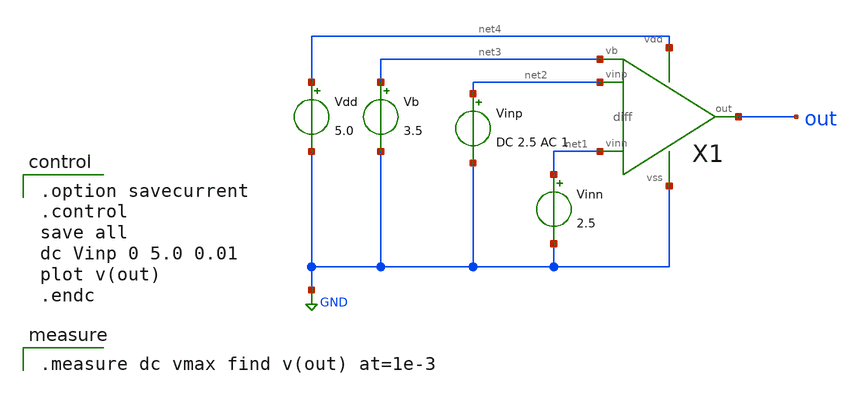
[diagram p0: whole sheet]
** sch_path: member_project/OPAMP/ShuntaroOhno/xschem/diff_dc.sch
**.subckt diff_dc
Vdd net4 GND 5.0
Vb net3 GND 3.5
Vinn net1 GND 2.5
Vinp net2 GND DC 2.5 AC 1
X1 net2 net1 out net4 GND net3 diff
**** begin user architecture code

.option savecurrent
.control
save all
dc Vinp 0 5.0 0.01
plot v(out)
.endc

 .include $::LIB/../ip62_models

.measure dc vmax find v(out) at=1e-3

**** end user architecture code
**.ends

* expanding   symbol:  diff.sym # of pins=6
** sym_path: diff.sym
** sch_path: diff.sch
.subckt diff vinp vinn out vdd vss vb
*.ipin vinn
*.ipin vinp
*.ipin vb
*.opin out
*.iopin vdd
*.iopin vss
XM5 net2 vb vdd vdd PMOS w=240u l=3u as=0 ad=0 ps=0 pd=0 nrd=0 nrs=0 m=1
XM1 net1 vinn net2 net2 PMOS w=720u l=3u as=0 ad=0 ps=0 pd=0 nrd=0 nrs=0 m=1
XM2 out vinp net2 net2 PMOS w=720u l=3u as=0 ad=0 ps=0 pd=0 nrd=0 nrs=0 m=1
XM3 net1 net1 vss vss NMOS w=60u l=3u as=0 ad=0 ps=0 pd=0 nrd=0 nrs=0 m=1
XM4 out net1 vss vss NMOS w=60u l=3u as=0 ad=0 ps=0 pd=0 nrd=0 nrs=0 m=1
.ends

.GLOBAL GND
.end
